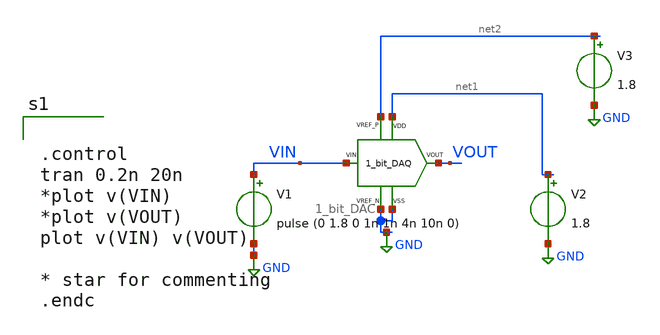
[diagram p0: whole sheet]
** sch_path: xschem/xschem_BGR_Top/Sigma_Delta/1_bit_DAC/1_bit_DAC_TB.sch
**.subckt 1_bit_DAC_TB
V1 VIN GND pulse (0 1.8 0 1n 1n 4n 10n 0)
V2 net1 GND 1.8
V3 net2 GND 1.8
X1 GND net1 VIN VOUT net2 GND 1_bit_DAC
**** begin user architecture code


.control
tran 0.2n 20n
*plot v(VIN)
*plot v(VOUT)
plot v(VIN) v(VOUT)

* star for commenting
.endc


** opencircuitdesign pdks install
.lib $::SKYWATER_MODELS/sky130.lib.spice tt


**** end user architecture code
**.ends

* expanding   symbol:  Sigma_Delta/1_bit_DAC/1_bit_DAC.sym # of pins=6
** sym_path: xschem/xschem_BGR_Top/Sigma_Delta/1_bit_DAC/1_bit_DAC.sym
** sch_path: xschem/xschem_BGR_Top/Sigma_Delta/1_bit_DAC/1_bit_DAC.sch
.subckt 1_bit_DAC VSS VDD VIN VOUT VREF_P VREF_N
*.iopin VIN
*.iopin VDD
*.iopin VSS
*.iopin VREF_P
*.iopin VREF_N
*.iopin VOUT
XM1 VOUT net1 VREF_N VSS sky130_fd_pr__nfet_01v8 L=0.15 W=0.6 nf=1 ad='int((nf+1)/2) * W/nf * 0.29' as='int((nf+2)/2) * W/nf * 0.29'
+ pd='2*int((nf+1)/2) * (W/nf + 0.29)' ps='2*int((nf+2)/2) * (W/nf + 0.29)' nrd='0.29 / W' nrs='0.29 / W'
+ sa=0 sb=0 sd=0 mult=1 m=1
XM3 VREF_P VIN VOUT VSS sky130_fd_pr__nfet_01v8 L=0.15 W=0.6 nf=1 ad='int((nf+1)/2) * W/nf * 0.29' as='int((nf+2)/2) * W/nf * 0.29'
+ pd='2*int((nf+1)/2) * (W/nf + 0.29)' ps='2*int((nf+2)/2) * (W/nf + 0.29)' nrd='0.29 / W' nrs='0.29 / W'
+ sa=0 sb=0 sd=0 mult=1 m=1
XM4 VREF_N VIN VOUT VDD sky130_fd_pr__pfet_01v8 L=0.15 W=0.8 nf=1 ad='int((nf+1)/2) * W/nf * 0.29' as='int((nf+2)/2) * W/nf * 0.29'
+ pd='2*int((nf+1)/2) * (W/nf + 0.29)' ps='2*int((nf+2)/2) * (W/nf + 0.29)' nrd='0.29 / W' nrs='0.29 / W'
+ sa=0 sb=0 sd=0 mult=1 m=1
X1 VSS VDD VIN net1 Inverter
XM2 VOUT net1 VREF_P VDD sky130_fd_pr__pfet_01v8 L=0.15 W=0.8 nf=1 ad='int((nf+1)/2) * W/nf * 0.29' as='int((nf+2)/2) * W/nf * 0.29'
+ pd='2*int((nf+1)/2) * (W/nf + 0.29)' ps='2*int((nf+2)/2) * (W/nf + 0.29)' nrd='0.29 / W' nrs='0.29 / W'
+ sa=0 sb=0 sd=0 mult=1 m=1
.ends


* expanding   symbol:  Sigma_Delta/Inverter/Inverter.sym # of pins=4
** sym_path: xschem/xschem_BGR_Top/Sigma_Delta/Inverter/Inverter.sym
** sch_path: xschem/xschem_BGR_Top/Sigma_Delta/Inverter/Inverter.sch
.subckt Inverter VSS VDD VIN VOUT
*.ipin VIN
*.iopin VDD
*.iopin VSS
*.opin VOUT
XM1 VOUT VIN VSS VSS sky130_fd_pr__nfet_01v8 L=0.15 W=0.9 nf=1 ad='int((nf+1)/2) * W/nf * 0.29' as='int((nf+2)/2) * W/nf * 0.29'
+ pd='2*int((nf+1)/2) * (W/nf + 0.29)' ps='2*int((nf+2)/2) * (W/nf + 0.29)' nrd='0.29 / W' nrs='0.29 / W'
+ sa=0 sb=0 sd=0 mult=1 m=1
XM2 VOUT VIN VDD VDD sky130_fd_pr__pfet_01v8 L=0.15 W=0.9 nf=2 ad='int((nf+1)/2) * W/nf * 0.29' as='int((nf+2)/2) * W/nf * 0.29'
+ pd='2*int((nf+1)/2) * (W/nf + 0.29)' ps='2*int((nf+2)/2) * (W/nf + 0.29)' nrd='0.29 / W' nrs='0.29 / W'
+ sa=0 sb=0 sd=0 mult=1 m=1
.ends

.GLOBAL GND
.end
